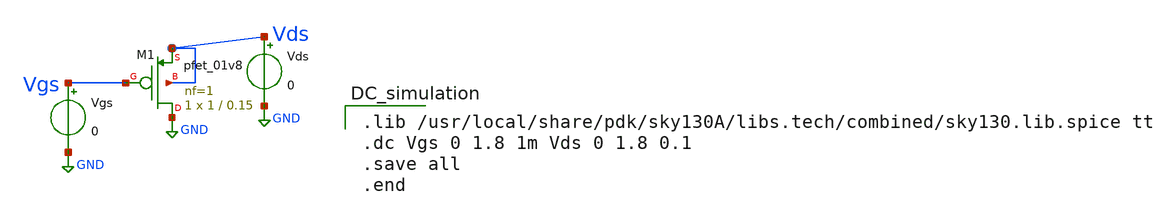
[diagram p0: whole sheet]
** sch_path: Circuit Files/circuits/circuits/dc_sweep.sch
**.subckt dc_sweep
Vds Vds GND 0
Vgs Vgs GND 0
XM1 GND Vgs Vds Vds sky130_fd_pr__pfet_01v8 L=0.15 W=1 nf=1 ad='int((nf+1)/2) * W/nf * 0.29' as='int((nf+2)/2) * W/nf * 0.29'
+ pd='2*int((nf+1)/2) * (W/nf + 0.29)' ps='2*int((nf+2)/2) * (W/nf + 0.29)' nrd='0.29 / W' nrs='0.29 / W'
+ sa=0 sb=0 sd=0 mult=1 m=1
**** begin user architecture code

.lib /usr/local/share/pdk/sky130A/libs.tech/combined/sky130.lib.spice tt
.dc Vgs 0 1.8 1m Vds 0 1.8 0.1
.save all
.end

**** end user architecture code
**.ends
.GLOBAL GND
.end
